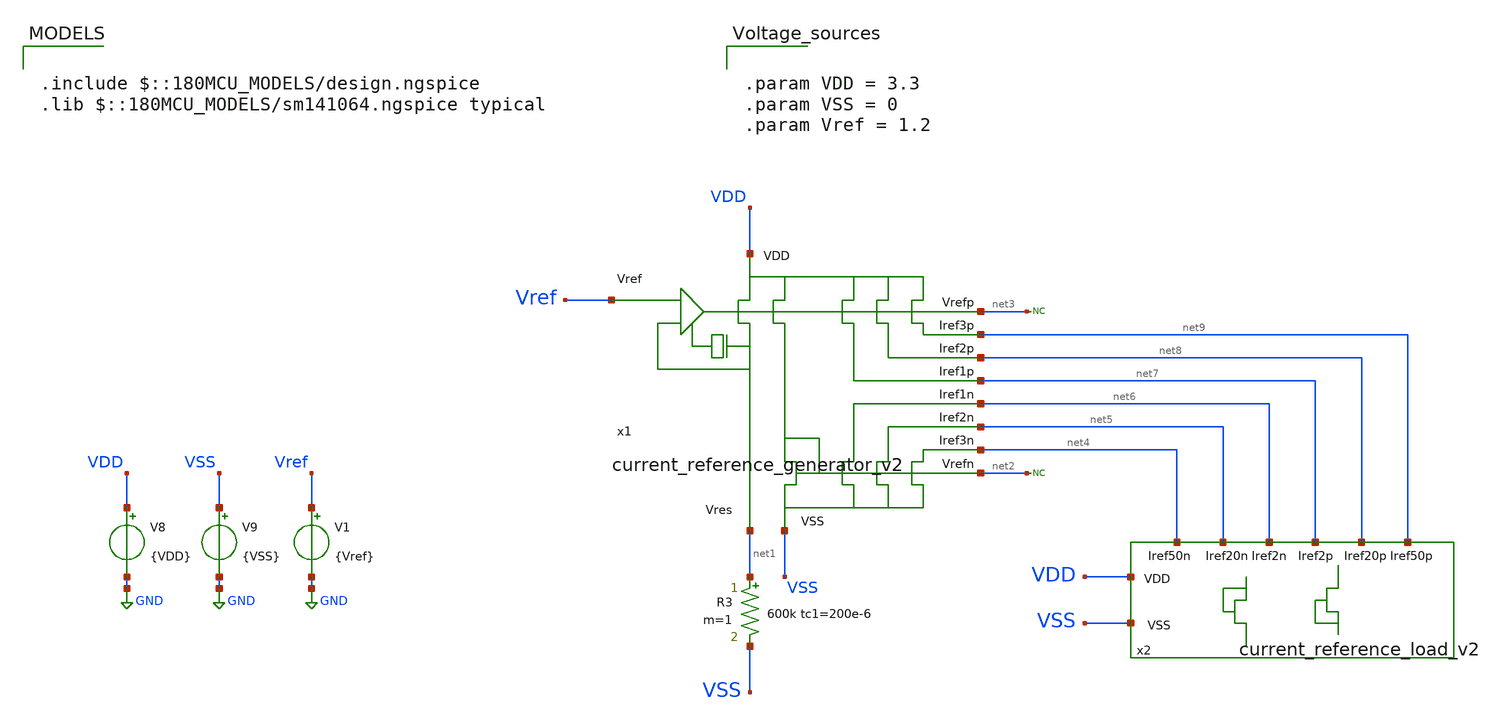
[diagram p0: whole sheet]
** sch_path: designs/libs/current_reference_generator_v2/xschem/current_reference_generator_v2_TB_temp.sch
**.subckt current_reference_generator_v2_TB_temp
V8 VDD GND {VDD}
V9 VSS GND {VSS}
V1 Vref GND {Vref}
R3 net1 VSS 600k tc1=200e-6 m=1
* noconn #net2
* noconn #net3
x1 VSS VDD Vref net3 net2 net6 net4 net7 net9 net1 net5 net8 current_reference_generator_v2
x2 net6 net4 net7 net9 VDD VSS net5 net8 current_reference_load_v2
**** begin user architecture code

.include $::180MCU_MODELS/design.ngspice
.lib $::180MCU_MODELS/sm141064.ngspice typical



.param VDD = 3.3
.param VSS = 0
.param Vref = 1.2





.save @m.x2.xm1.m0[id]
.save @m.x2.xm2.m0[id]
.save @m.x2.xm3.m0[id]
.save @m.x2.xm4.m0[id]
.save @m.x2.xm5.m0[id]
.save @m.x2.xm6.m0[id]

.control
save all

** OP simulation
op

** Temp simulation
dc temp -40 125 1

** All OP parameters
setplot op1

** Error amplifier core
let ##########_Error_amplifier_op_########## = 1
print ##########_Error_amplifier_op_##########

let #####_M1_nmos_input_##### = 0
let id_M1 = @m.x1.x1.x1.xm1.m0[id]
let gm_M1 = @m.x1.x1.x1.xm1.m0[gm]
let ro_M1 = 1/@m.x1.x1.x1.xm1.m0[gds]
let Vgs_M1 = @m.x1.x1.x1.xm1.m0[vgs]
let Vds_M1 = @m.x1.x1.x1.xm1.m0[vds]
let Vsb_M1 = -@m.x1.x1.x1.xm1.m0[vbs]
let Vdsat_M1 = @m.x1.x1.x1.xm1.m0[vdsat]
let Vth_M1 = @m.x1.x1.x1.xm1.m0[vth]
let ao_M1 = gm_M1*ro_M1
let gmid_M1 = gm_M1/id_M1
let fT_M1 = gm_M1/(6.283185*@m.x1.x1.x1.xm1.m0[cgg])
print #####_M1_nmos_input_##### id_M1 gm_M1 ro_M1 Vgs_M1 Vds_M1 Vsb_M1 Vdsat_M1 Vth_M1 ao_M1 gmid_M1
+ fT_M1

let #####_M2_nmos_input_##### = 0
let id_M2 = @m.x1.x1.x1.xm2.m0[id]
let gm_M2 = @m.x1.x1.x1.xm2.m0[gm]
let ro_M2 = 1/@m.x1.x1.x1.xm2.m0[gds]
let Vgs_M2 = @m.x1.x1.x1.xm2.m0[vgs]
let Vds_M2 = @m.x1.x1.x1.xm2.m0[vds]
let Vsb_M2 = -@m.x1.x1.x1.xm2.m0[vbs]
let Vdsat_M2 = @m.x1.x1.x1.xm2.m0[vdsat]
let Vth_M2 = @m.x1.x1.x1.xm2.m0[vth]
let ao_M2 = gm_M2*ro_M2
let gmid_M2 = gm_M2/id_M2
let fT_M2 = gm_M2/(6.283185*@m.x1.x1.x1.xm2.m0[cgg])
print #####_M2_nmos_input_##### id_M2 gm_M2 ro_M2 Vgs_M2 Vds_M2 Vsb_M2 Vdsat_M2 Vth_M2 ao_M2 gmid_M2
+ fT_M2

let #####_M3_pmos_top_##### = 0
let id_M3 = @m.x1.x1.x1.xm3.m0[id]
let gm_M3 = @m.x1.x1.x1.xm3.m0[gm]
let ro_M3 = 1/@m.x1.x1.x1.xm3.m0[gds]
let Vsg_M3 = @m.x1.x1.x1.xm3.m0[vgs]
let Vsd_M3 = @m.x1.x1.x1.xm3.m0[vds]
let Vbs_M3 = -@m.x1.x1.x1.xm3.m0[vbs]
let Vdsat_M3 = @m.x1.x1.x1.xm3.m0[vdsat]
let Vth_M3 = @m.x1.x1.x1.xm3.m0[vth]
let ao_M3 = gm_M3*ro_M3
let gmid_M3 = gm_M3/id_M3
let fT_M3 = gm_M3/(6.283185*@m.x1.x1.x1.xm3.m0[cgg])
print #####_M3_pmos_top_##### id_M3 gm_M3 ro_M3 Vsg_M3 Vsd_M3 Vbs_M3 Vdsat_M3 Vth_M3 ao_M3 gmid_M3
+ fT_M3

let #####_M4_pmos_top_##### = 0
let id_M4 = @m.x1.x1.x1.xm4.m0[id]
let gm_M4 = @m.x1.x1.x1.xm4.m0[gm]
let ro_M4 = 1/@m.x1.x1.x1.xm4.m0[gds]
let Vsg_M4 = @m.x1.x1.x1.xm4.m0[vgs]
let Vsd_M4 = @m.x1.x1.x1.xm4.m0[vds]
let Vbs_M4 = -@m.x1.x1.x1.xm4.m0[vbs]
let Vdsat_M4 = @m.x1.x1.x1.xm4.m0[vdsat]
let Vth_M4 = @m.x1.x1.x1.xm4.m0[vth]
let ao_M4 = gm_M4*ro_M4
let gmid_M4 = gm_M4/id_M4
let fT_M4 = gm_M4/(6.283185*@m.x1.x1.x1.xm4.m0[cgg])
print #####_M4_pmos_top_##### id_M4 gm_M4 ro_M4 Vsg_M4 Vsd_M4 Vbs_M4 Vdsat_M4 Vth_M4 ao_M4 gmid_M4
+ fT_M4

let #####_M5_pmos_out_##### = 0
let id_M5 = @m.x1.x1.x1.xm5.m0[id]
let gm_M5 = @m.x1.x1.x1.xm5.m0[gm]
let ro_M5 = 1/@m.x1.x1.x1.xm5.m0[gds]
let Vsg_M5 = @m.x1.x1.x1.xm5.m0[vgs]
let Vsd_M5 = @m.x1.x1.x1.xm5.m0[vds]
let Vbs_M5 = -@m.x1.x1.x1.xm5.m0[vbs]
let Vdsat_M5 = @m.x1.x1.x1.xm5.m0[vdsat]
let Vth_M5 = @m.x1.x1.x1.xm5.m0[vth]
let ao_M5 = gm_M5*ro_M5
let gmid_M5 = gm_M5/id_M5
let fT_M5 = gm_M5/(6.283185*@m.x1.x1.x1.xm5.m0[cgg])
print #####_M5_pmos_out_##### id_M5 gm_M5 ro_M5 Vsg_M5 Vsd_M5 Vbs_M5 Vdsat_M5 Vth_M5 ao_M5 gmid_M5
+ fT_M5

let #####_M6_pmos_out_##### = 0
let id_M6 = @m.x1.x1.x1.xm6.m0[id]
let gm_M6 = @m.x1.x1.x1.xm6.m0[gm]
let ro_M6 = 1/@m.x1.x1.x1.xm6.m0[gds]
let Vsg_M6 = @m.x1.x1.x1.xm6.m0[vgs]
let Vsd_M6 = @m.x1.x1.x1.xm6.m0[vds]
let Vbs_M6 = -@m.x1.x1.x1.xm6.m0[vbs]
let Vdsat_M6 = @m.x1.x1.x1.xm6.m0[vdsat]
let Vth_M6 = @m.x1.x1.x1.xm6.m0[vth]
let ao_M6 = gm_M6*ro_M6
let gmid_M6 = gm_M6/id_M6
let fT_M6 = gm_M6/(6.283185*@m.x1.x1.x1.xm6.m0[cgg])
print #####_M6_pmos_out_##### id_M6 gm_M6 ro_M6 Vsg_M6 Vsd_M6 Vbs_M6 Vdsat_M6 Vth_M6 ao_M6 gmid_M6
+ fT_M6

let #####_M7_nmos_out_##### = 0
let id_M7 = @m.x1.x1.x1.xm7.m0[id]
let gm_M7 = @m.x1.x1.x1.xm7.m0[gm]
let ro_M7 = 1/@m.x1.x1.x1.xm7.m0[gds]
let Vgs_M7 = @m.x1.x1.x1.xm7.m0[vgs]
let Vds_M7 = @m.x1.x1.x1.xm7.m0[vds]
let Vsb_M7 = -@m.x1.x1.x1.xm7.m0[vbs]
let Vdsat_M7 = @m.x1.x1.x1.xm7.m0[vdsat]
let Vth_M7 = @m.x1.x1.x1.xm7.m0[vth]
let ao_M7 = gm_M7*ro_M7
let gmid_M7 = gm_M7/id_M7
let fT_M7 = gm_M7/(6.283185*@m.x1.x1.x1.xm7.m0[cgg])
print #####_M7_nmos_out_##### id_M7 gm_M7 ro_M7 Vgs_M7 Vds_M7 Vsb_M7 Vdsat_M7 Vth_M7 ao_M7 gmid_M7
+ fT_M7

let #####_M8_nmos_out_##### = 0
let id_M8 = @m.x1.x1.x1.xm8.m0[id]
let gm_M8 = @m.x1.x1.x1.xm8.m0[gm]
let ro_M8 = 1/@m.x1.x1.x1.xm8.m0[gds]
let Vgs_M8 = @m.x1.x1.x1.xm8.m0[vgs]
let Vds_M8 = @m.x1.x1.x1.xm8.m0[vds]
let Vsb_M8 = -@m.x1.x1.x1.xm8.m0[vbs]
let Vdsat_M8 = @m.x1.x1.x1.xm8.m0[vdsat]
let Vth_M8 = @m.x1.x1.x1.xm8.m0[vth]
let ao_M8 = gm_M8*ro_M8
let gmid_M8 = gm_M8/id_M8
let fT_M8 = gm_M8/(6.283185*@m.x1.x1.x1.xm8.m0[cgg])
print #####_M8_nmos_out_##### id_M8 gm_M8 ro_M8 Vgs_M8 Vds_M8 Vsb_M8 Vdsat_M8 Vth_M8 ao_M8 gmid_M8
+ fT_M8

let #####_M9_nmos_bottom_##### = 0
let id_M9 = @m.x1.x1.x1.xm9.m0[id]
let gm_M9 = @m.x1.x1.x1.xm9.m0[gm]
let ro_M9 = 1/@m.x1.x1.x1.xm9.m0[gds]
let Vgs_M9 = @m.x1.x1.x1.xm9.m0[vgs]
let Vds_M9 = @m.x1.x1.x1.xm9.m0[vds]
let Vsb_M9 = -@m.x1.x1.x1.xm9.m0[vbs]
let Vdsat_M9 = @m.x1.x1.x1.xm9.m0[vdsat]
let Vth_M9 = @m.x1.x1.x1.xm9.m0[vth]
let ao_M9 = gm_M9*ro_M9
let gmid_M9 = gm_M9/id_M9
let fT_M9 = gm_M9/(6.283185*@m.x1.x1.x1.xm9.m0[cgg])
print #####_M9_nmos_bottom_##### id_M9 gm_M9 ro_M9 Vgs_M9 Vds_M9 Vsb_M9 Vdsat_M9 Vth_M9 ao_M9
+ gmid_M9 fT_M9

let #####_M10_nmos_bottom_##### = 0
let id_M10 = @m.x1.x1.x1.xm10.m0[id]
let gm_M10 = @m.x1.x1.x1.xm10.m0[gm]
let ro_M10 = 1/@m.x1.x1.x1.xm10.m0[gds]
let Vgs_M10 = @m.x1.x1.x1.xm10.m0[vgs]
let Vds_M10 = @m.x1.x1.x1.xm10.m0[vds]
let Vsb_M10 = @m.x1.x1.x1.xm10.m0[vbs]
let Vdsat_M10 = @m.x1.x1.x1.xm10.m0[vdsat]
let Vth_M10 = @m.x1.x1.x1.xm10.m0[vth]
let ao_M10 = gm_M10*ro_M10
let gmid_M10 = gm_M10/id_M10
let fT_M10 = gm_M10/(6.283185*@m.x1.x1.x1.xm10.m0[cgg])
print #####_M10_nmos_bottom_##### id_M10 gm_M10 ro_M10 Vgs_M10 Vds_M10 Vsb_M10 Vdsat_M10 Vth_M10
+ ao_M10 gmid_M10 fT_M10

let #####_M11_nmos_mirror_##### = 0
let id_M11 = @m.x1.x1.x1.xm11.m0[id]
let gm_M11 = @m.x1.x1.x1.xm11.m0[gm]
let ro_M11 = 1/@m.x1.x1.x1.xm11.m0[gds]
let Vgs_M11 = @m.x1.x1.x1.xm11.m0[vgs]
let Vds_M11 = @m.x1.x1.x1.xm11.m0[vds]
let Vsb_M11 = -@m.x1.x1.x1.xm11.m0[vbs]
let Vdsat_M11 = @m.x1.x1.x1.xm11.m0[vdsat]
let Vth_M11 = @m.x1.x1.x1.xm11.m0[vth]
let ao_M11 = gm_M11*ro_M11
let gmid_M11 = gm_M11/id_M11
let fT_M11 = gm_M11/(6.283185*@m.x1.x1.x1.xm11.m0[cgg])
print #####_M11_nmos_mirror_##### id_M11 gm_M11 ro_M11 Vgs_M11 Vds_M11 Vsb_M11 Vdsat_M11 Vth_M11
+ ao_M11 gmid_M11 fT_M11

** Second stage
let ##########_Second_stage_op_########## = 1
print ##########_Second_stage_op_##########

let #####_M1_pmos_##### = 0
let id_M1 = @m.x1.x2.xm1.m0[id]
let gm_M1 = @m.x1.x2.xm1.m0[gm]
let ro_M1 = 1/@m.x1.x2.xm1.m0[gds]
let Vsg_M1 = @m.x1.x2.xm1.m0[vgs]
let Vsd_M1 = @m.x1.x2.xm1.m0[vds]
let Vbs_M1 = -@m.x1.x2.xm1.m0[vbs]
let Vdsat_M1 = @m.x1.x2.xm1.m0[vdsat]
let Vth_M1 = @m.x1.x2.xm1.m0[vth]
let ao_M1 = gm_M1*ro_M1
let gmid_M1 = gm_M1/id_M1
let fT_M1 = gm_M1/(6.283185*@m.x1.x2.xm1.m0[cgg])
print #####_M1_pmos_##### id_M1 gm_M1 ro_M1 Vsg_M1 Vsd_M1 Vbs_M1 Vdsat_M1 Vth_M1 ao_M1 gmid_M1 fT_M1

let #####_M2_pmos_##### = 0
let id_M2 = @m.x1.x2.xm2.m0[id]
let gm_M2 = @m.x1.x2.xm2.m0[gm]
let ro_M2 = 1/@m.x1.x2.xm2.m0[gds]
let Vsg_M2 = @m.x1.x2.xm2.m0[vgs]
let Vsd_M2 = @m.x1.x2.xm2.m0[vds]
let Vbs_M2 = -@m.x1.x2.xm2.m0[vbs]
let Vdsat_M2 = @m.x1.x2.xm2.m0[vdsat]
let Vth_M2 = @m.x1.x2.xm2.m0[vth]
let ao_M2 = gm_M2*ro_M2
let gmid_M2 = gm_M2/id_M2
let fT_M2 = gm_M2/(6.283185*@m.x1.x2.xm2.m0[cgg])
print #####_M2_pmos_##### id_M2 gm_M2 ro_M2 Vsg_M2 Vsd_M2 Vbs_M2 Vdsat_M2 Vth_M2 ao_M2 gmid_M2 fT_M2

let #####_M3_pmos_##### = 0
let id_M3 = @m.x1.x2.xm3.m0[id]
let gm_M3 = @m.x1.x2.xm3.m0[gm]
let ro_M3 = 1/@m.x1.x2.xm3.m0[gds]
let Vsg_M3 = @m.x1.x2.xm3.m0[vgs]
let Vsd_M3 = @m.x1.x2.xm3.m0[vds]
let Vbs_M3 = -@m.x1.x2.xm3.m0[vbs]
let Vdsat_M3 = @m.x1.x2.xm3.m0[vdsat]
let Vth_M3 = @m.x1.x2.xm3.m0[vth]
let ao_M3 = gm_M3*ro_M3
let gmid_M3 = gm_M3/id_M3
let fT_M3 = gm_M3/(6.283185*@m.x1.x2.xm3.m0[cgg])
print #####_M3_pmos_##### id_M3 gm_M3 ro_M3 Vsg_M3 Vsd_M3 Vbs_M3 Vdsat_M3 Vth_M3 ao_M3 gmid_M3 fT_M3

let #####_M4_pmos_##### = 0
let id_M4 = @m.x1.x2.xm4.m0[id]
let gm_M4 = @m.x1.x2.xm4.m0[gm]
let ro_M4 = 1/@m.x1.x2.xm4.m0[gds]
let Vsg_M4 = @m.x1.x2.xm4.m0[vgs]
let Vsd_M4 = @m.x1.x2.xm4.m0[vds]
let Vbs_M4 = -@m.x1.x2.xm4.m0[vbs]
let Vdsat_M4 = @m.x1.x2.xm4.m0[vdsat]
let Vth_M4 = @m.x1.x2.xm4.m0[vth]
let ao_M4 = gm_M4*ro_M4
let gmid_M4 = gm_M4/id_M4
let fT_M4 = gm_M4/(6.283185*@m.x1.x2.xm4.m0[cgg])
print #####_M4_pmos_##### id_M4 gm_M4 ro_M4 Vsg_M4 Vsd_M4 Vbs_M4 Vdsat_M4 Vth_M4 ao_M4 gmid_M4 fT_M4

let #####_M5_pmos_##### = 0
let id_M5 = @m.x1.x2.xm5.m0[id]
let gm_M5 = @m.x1.x2.xm5.m0[gm]
let ro_M5 = 1/@m.x1.x2.xm5.m0[gds]
let Vsg_M5 = @m.x1.x2.xm5.m0[vgs]
let Vsd_M5 = @m.x1.x2.xm5.m0[vds]
let Vbs_M5 = -@m.x1.x2.xm5.m0[vbs]
let Vdsat_M5 = @m.x1.x2.xm5.m0[vdsat]
let Vth_M5 = @m.x1.x2.xm5.m0[vth]
let ao_M5 = gm_M5*ro_M5
print #####_M5_pmos_##### id_M5 gm_M5 ro_M5 Vsg_M5 Vsd_M5 Vbs_M5 Vdsat_M5 Vth_M5 ao_M5 gmid_M5

let #####_M6_nmos_##### = 0
let id_M6 = @m.x1.x2.xm6.m0[id]
let gm_M6 = @m.x1.x2.xm6.m0[gm]
let ro_M6 = 1/@m.x1.x2.xm6.m0[gds]
let Vgs_M6 = @m.x1.x2.xm6.m0[vgs]
let Vds_M6 = @m.x1.x2.xm6.m0[vds]
let Vsb_M6 = -@m.x1.x2.xm6.m0[vbs]
let Vdsat_M6 = @m.x1.x2.xm6.m0[vdsat]
let Vth_M6 = @m.x1.x2.xm6.m0[vth]
let ao_M6 = gm_M6*ro_M6
let gmid_M6 = gm_M6/id_M6
let fT_M6 = gm_M6/(6.283185*@m.x1.x2.xm6.m0[cgg])
print #####_M6_nmos_##### id_M6 gm_M6 ro_M6 Vgs_M6 Vds_M6 Vsb_M6 Vdsat_M6 Vth_M6 ao_M6 gmid_M6 fT_M6

let #####_M7_nmos_##### = 0
let id_M7 = @m.x1.x2.xm7.m0[id]
let gm_M7 = @m.x1.x2.xm7.m0[gm]
let ro_M7 = 1/@m.x1.x2.xm7.m0[gds]
let Vgs_M7 = @m.x1.x2.xm7.m0[vgs]
let Vds_M7 = @m.x1.x2.xm7.m0[vds]
let Vsb_M7 = -@m.x1.x2.xm7.m0[vbs]
let Vdsat_M7 = @m.x1.x2.xm7.m0[vdsat]
let Vth_M7 = @m.x1.x2.xm7.m0[vth]
let ao_M7 = gm_M7*ro_M7
let gmid_M7 = gm_M7/id_M7
let fT_M7 = gm_M7/(6.283185*@m.x1.x2.xm7.m0[cgg])
print #####_M7_nmos_##### id_M7 gm_M7 ro_M7 Vgs_M7 Vds_M7 Vsb_M7 Vdsat_M7 Vth_M7 ao_M7 gmid_M7 fT_M7

let #####_M8_nmos_##### = 0
let id_M8 = @m.x1.x2.xm8.m0[id]
let gm_M8 = @m.x1.x2.xm8.m0[gm]
let ro_M8 = 1/@m.x1.x2.xm8.m0[gds]
let Vgs_M8 = @m.x1.x2.xm8.m0[vgs]
let Vds_M8 = @m.x1.x2.xm8.m0[vds]
let Vsb_M8 = -@m.x1.x2.xm8.m0[vbs]
let Vdsat_M8 = @m.x1.x2.xm8.m0[vdsat]
let Vth_M8 = @m.x1.x2.xm8.m0[vth]
let ao_M8 = gm_M8*ro_M8
let gmid_M8 = gm_M8/id_M8
let fT_M8 = gm_M8/(6.283185*@m.x1.x2.xm8.m0[cgg])
print #####_M8_nmos_##### id_M8 gm_M8 ro_M8 Vgs_M8 Vds_M8 Vsb_M8 Vdsat_M8 Vth_M8 ao_M8 gmid_M8 fT_M8

** Load
let ##########_Load_op_########## = 1
print ##########_Load_op_##########

let #####_M1_pmos_##### = 0
let id_M1 = @m.x3.xm1.m0[id]
let gm_M1 = @m.x3.xm1.m0[gm]
let ro_M1 = 1/@m.x3.xm1.m0[gds]
let Vsg_M1 = @m.x3.xm1.m0[vgs]
let Vsd_M1 = @m.x3.xm1.m0[vds]
let Vbs_M1 = -@m.x3.xm1.m0[vbs]
let Vdsat_M1 = @m.x3.xm1.m0[vdsat]
let Vth_M1 = @m.x3.xm1.m0[vth]
let ao_M1 = gm_M1*ro_M1
let gmid_M1 = gm_M1/id_M1
let fT_M1 = gm_M1/(6.283185*@m.x3.xm1.m0[cgg])
print #####_M1_pmos_##### id_M1 gm_M1 ro_M1 Vsg_M1 Vsd_M1 Vbs_M1 Vdsat_M1 Vth_M1 ao_M1 gmid_M1 fT_M1

let #####_M2_pmos_##### = 0
let id_M2 = @m.x3.xm2.m0[id]
let gm_M2 = @m.x3.xm2.m0[gm]
let ro_M2 = 1/@m.x3.xm2.m0[gds]
let Vsg_M2 = @m.x3.xm2.m0[vgs]
let Vsd_M2 = @m.x3.xm2.m0[vds]
let Vbs_M2 = -@m.x3.xm2.m0[vbs]
let Vdsat_M2 = @m.x3.xm2.m0[vdsat]
let Vth_M2 = @m.x3.xm2.m0[vth]
let ao_M2 = gm_M2*ro_M2
let gmid_M2 = gm_M2/id_M2
let fT_M2 = gm_M2/(6.283185*@m.x3.xm2.m0[cgg])
print #####_M2_pmos_##### id_M2 gm_M2 ro_M2 Vsg_M2 Vsd_M2 Vbs_M2 Vdsat_M2 Vth_M2 ao_M2 gmid_M2 fT_M2

let #####_M3_nmos_##### = 0
let id_M3 = @m.x3.xm3.m0[id]
let gm_M3 = @m.x3.xm3.m0[gm]
let ro_M3 = 1/@m.x3.xm3.m0[gds]
let Vgs_M3 = @m.x3.xm3.m0[vgs]
let Vds_M3 = @m.x3.xm3.m0[vds]
let Vsb_M3 = -@m.x3.xm3.m0[vbs]
let Vdsat_M3 = @m.x3.xm3.m0[vdsat]
let Vth_M3 = @m.x3.xm3.m0[vth]
let ao_M3 = gm_M3*ro_M3
let gmid_M3 = gm_M3/id_M3
let fT_M3 = gm_M3/(6.283185*@m.x3.xm3.m0[cgg])
print #####_M3_nmos_##### id_M3 gm_M3 ro_M3 Vgs_M3 Vds_M3 Vsb_M3 Vdsat_M3 Vth_M3 ao_M3 gmid_M3 fT_M3

let #####_M4_nmos_##### = 0
let id_M4 = @m.x3.xm4.m0[id]
let gm_M4 = @m.x3.xm4.m0[gm]
let ro_M4 = 1/@m.x3.xm4.m0[gds]
let Vgs_M4 = @m.x3.xm4.m0[vgs]
let Vds_M4 = @m.x3.xm4.m0[vds]
let Vsb_M4 = -@m.x3.xm4.m0[vbs]
let Vdsat_M4 = @m.x3.xm4.m0[vdsat]
let Vth_M4 = @m.x3.xm4.m0[vth]
let ao_M4 = gm_M4*ro_M4
let gmid_M4 = gm_M4/id_M4
let fT_M4 = gm_M4/(6.283185*@m.x3.xm4.m0[cgg])
print #####_M4_nmos_##### id_M4 gm_M4 ro_M4 Vgs_M4 Vds_M4 Vsb_M4 Vdsat_M4 Vth_M4 ao_M4 gmid_M4 fT_M4

** Custom output
let #####_Custom_output_##### = 0

* Power
let power = abs(i(V8))*VDD

* DC_gain
let r1 = ao_M6*ro_M4
let r2 = ao_M8*((ro_M1*ro_M10)/(ro_M1+ro_M10))
let Rout = (r1*r2)/(r1+r2)
let Av = db(gm_M1*Rout)
* Bandwidth
let BW = 1/(Rout*1e-12*6.283185)

print #####_Custom_output_##### Av BW Rout power gm_M1 ro_M1 gm_M6 ro_M6 ro_M4 gm_M8 ro_M8 ro_M10

write current_reference_generator_v2_TB_temp.raw

* Temp results
setplot dc1
let id_n2 = @m.x2.xm1.m0[id]
let id_n20 = @m.x2.xm2.m0[id]
let id_n50 = @m.x2.xm3.m0[id]
let id_p2 = @m.x2.xm4.m0[id]
let id_p20 = @m.x2.xm5.m0[id]
let id_p50 = @m.x2.xm6.m0[id]
plot id_n2 id_p2
plot id_n20 id_p20
plot id_n50 id_p50

.endc



**** end user architecture code
**.ends
.GLOBAL GND
.end
